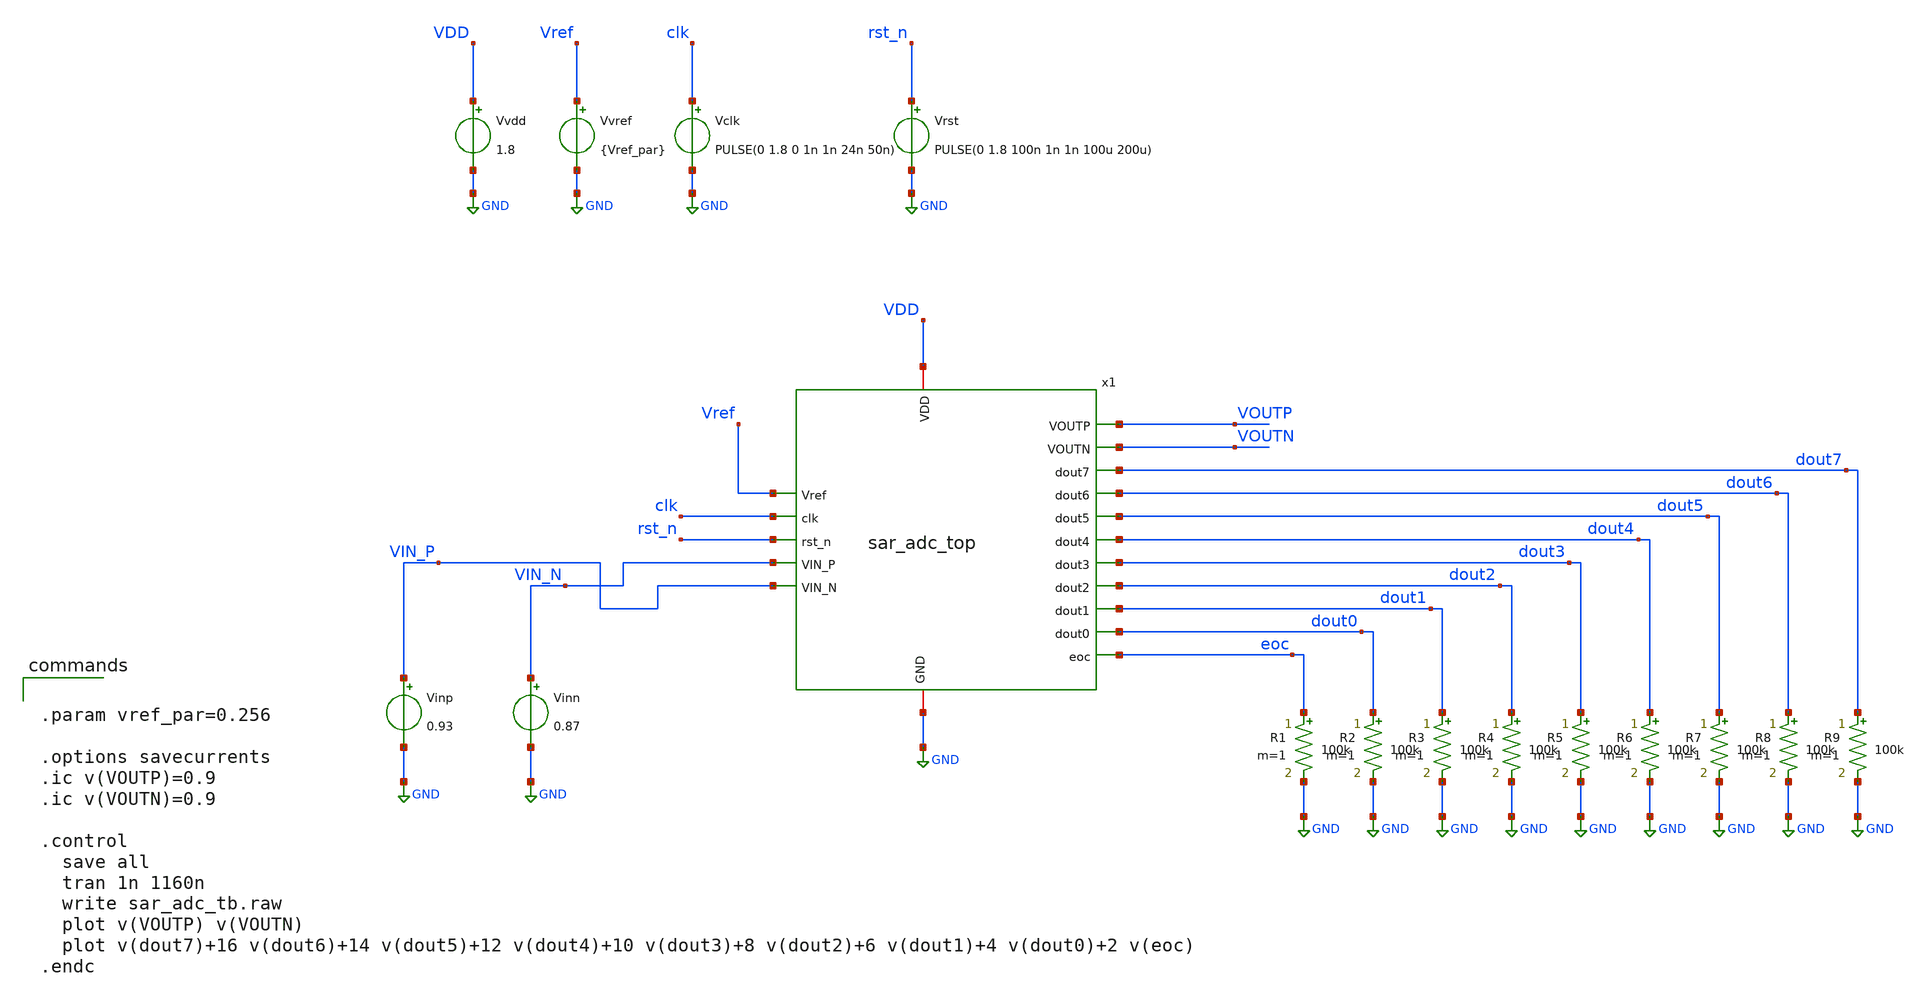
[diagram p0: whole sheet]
** sch_path: 05_mixed_signal/soluzioni/lab03/xschem/sar_adc_tb.sch
**.subckt sar_adc_tb
x1 VDD GND Vref VOUTP VOUTN clk rst_n VIN_N dout7 dout6 dout5 dout4 dout3 dout2 dout1 dout0 VIN_P
+ eoc sar_adc_top
Vvdd VDD GND 1.8
Vvref Vref GND {Vref_par}
Vclk clk GND PULSE(0 1.8 0 1n 1n 24n 50n)
Vrst rst_n GND PULSE(0 1.8 100n 1n 1n 100u 200u)
R1 eoc GND 100k m=1
R2 dout0 GND 100k m=1
R3 dout1 GND 100k m=1
R4 dout2 GND 100k m=1
R5 dout3 GND 100k m=1
R6 dout4 GND 100k m=1
R7 dout5 GND 100k m=1
R8 dout6 GND 100k m=1
R9 dout7 GND 100k m=1
Vinp VIN_P GND 0.93
Vinn VIN_N GND 0.87
**** begin user architecture code

** opencircuitdesign pdks install
.lib $::SKYWATER_MODELS/sky130.lib.spice tt



.param vref_par=0.256

.options savecurrents
.ic v(VOUTP)=0.9
.ic v(VOUTN)=0.9

.control
  save all
  tran 1n 1160n
  write sar_adc_tb.raw
  plot v(VOUTP) v(VOUTN)
  plot v(dout7)+16 v(dout6)+14 v(dout5)+12 v(dout4)+10 v(dout3)+8 v(dout2)+6 v(dout1)+4 v(dout0)+2
+ v(eoc)
.endc


**** end user architecture code
**.ends
.GLOBAL GND
.end
